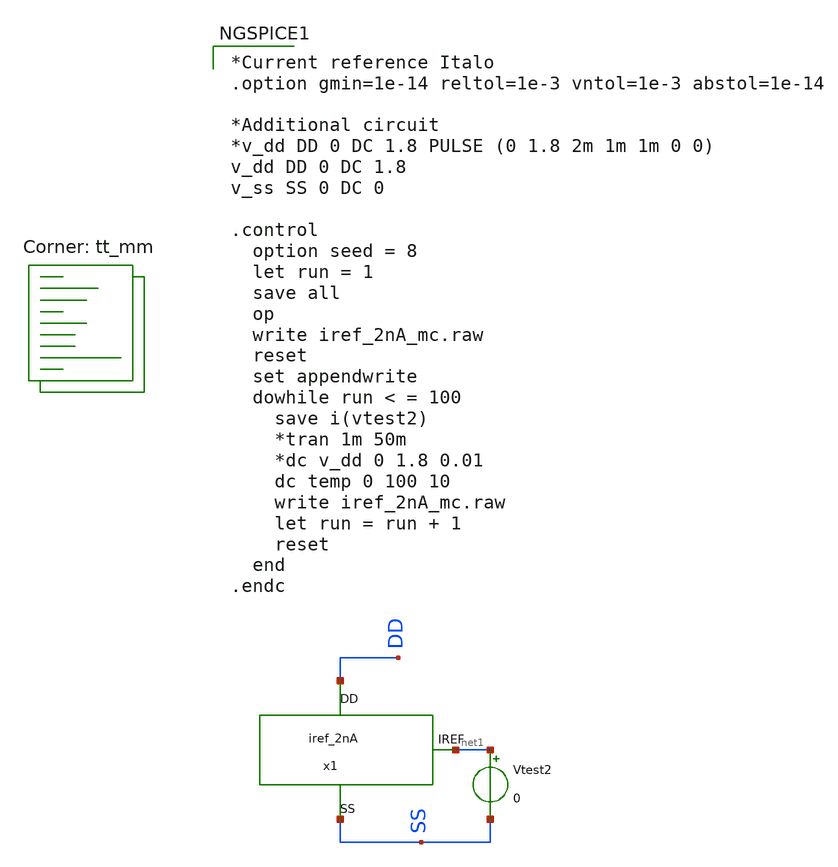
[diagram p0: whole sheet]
** sch_path: xschem/test_iref_2nA_mc.sch
**.subckt test_iref_2nA_mc
x1 net1 DD SS iref_2nA
Vtest2 net1 SS 0
**** begin user architecture code
.lib $::SKYWATER_MODELS/sky130.lib.spice tt_mm

*Current reference Italo
.option gmin=1e-14 reltol=1e-3 vntol=1e-3 abstol=1e-14

*Additional circuit
*v_dd DD 0 DC 1.8 PULSE (0 1.8 2m 1m 1m 0 0)
v_dd DD 0 DC 1.8
v_ss SS 0 DC 0

.control
  option seed = 8
  let run = 1
  save all
  op
  write iref_2nA_mc.raw
  reset
  set appendwrite
  dowhile run < = 100
    save i(vtest2)
    *tran 1m 50m
    *dc v_dd 0 1.8 0.01
    dc temp 0 100 10
    write iref_2nA_mc.raw
    let run = run + 1
    reset
  end
.endc


**** end user architecture code
**.ends

* expanding   symbol:  iref_2nA.sym # of pins=3
** sym_path: xschem/iref_2nA.sym
** sch_path: xschem/iref_2nA.sch
.subckt iref_2nA IREF DD SS
*.iopin DD
*.iopin SS
*.iopin IREF
x1 net3 SS net1 VCTAT net2 iref_2nA_igenerator
x3 DD SS net1 net2 net3 IREF iref_2nA_mirrors
x2 VCTAT DD SS iref_2nA_vref
.ends


* expanding   symbol:  iref_2nA_igenerator.sym # of pins=5
** sym_path: xschem/iref_2nA_igenerator.sym
** sch_path: xschem/iref_2nA_igenerator.sch
.subckt iref_2nA_igenerator Ip2 SS Ip1 VCTAT Vg
*.iopin SS
*.ipin VCTAT
*.iopin Ip1
*.iopin Vg
*.iopin Ip2
XM1 Ip1 Vg VPTAT SS sky130_fd_pr__nfet_01v8_lvt L=1 W=2.5 nf=1 ad='int((nf+1)/2) * W/nf * 0.29' as='int((nf+2)/2) * W/nf * 0.29'
+ pd='2*int((nf+1)/2) * (W/nf + 0.29)' ps='2*int((nf+2)/2) * (W/nf + 0.29)' nrd='0.29 / W' nrs='0.29 / W'
+ sa=0 sb=0 sd=0 mult=2 m=2
XM2 Ip2 Vg SS SS sky130_fd_pr__nfet_01v8_lvt L=1 W=2.5 nf=1 ad='int((nf+1)/2) * W/nf * 0.29' as='int((nf+2)/2) * W/nf * 0.29'
+ pd='2*int((nf+1)/2) * (W/nf + 0.29)' ps='2*int((nf+2)/2) * (W/nf + 0.29)' nrd='0.29 / W' nrs='0.29 / W'
+ sa=0 sb=0 sd=0 mult=2 m=2
XM3 VPTAT VCTAT SS SS sky130_fd_pr__nfet_01v8_lvt L=5 W=1 nf=1 ad='int((nf+1)/2) * W/nf * 0.29' as='int((nf+2)/2) * W/nf * 0.29'
+ pd='2*int((nf+1)/2) * (W/nf + 0.29)' ps='2*int((nf+2)/2) * (W/nf + 0.29)' nrd='0.29 / W' nrs='0.29 / W'
+ sa=0 sb=0 sd=0 mult=1 m=1
XM4 SS SS SS SS sky130_fd_pr__nfet_01v8_lvt L=1 W=2.5 nf=1 ad='int((nf+1)/2) * W/nf * 0.29' as='int((nf+2)/2) * W/nf * 0.29'
+ pd='2*int((nf+1)/2) * (W/nf + 0.29)' ps='2*int((nf+2)/2) * (W/nf + 0.29)' nrd='0.29 / W' nrs='0.29 / W'
+ sa=0 sb=0 sd=0 mult=2 m=2
.ends


* expanding   symbol:  iref_2nA_mirrors.sym # of pins=6
** sym_path: xschem/iref_2nA_mirrors.sym
** sch_path: xschem/iref_2nA_mirrors.sch
.subckt iref_2nA_mirrors DD SS Ip1 Vg Ip2 Iref
*.iopin DD
*.iopin SS
*.iopin Iref
*.iopin Ip2
*.iopin Vg
*.iopin Ip1
XM7 net3 Ip2 DD DD sky130_fd_pr__pfet_01v8_lvt L=2 W=2.5 nf=1 ad='int((nf+1)/2) * W/nf * 0.29' as='int((nf+2)/2) * W/nf * 0.29'
+ pd='2*int((nf+1)/2) * (W/nf + 0.29)' ps='2*int((nf+2)/2) * (W/nf + 0.29)' nrd='0.29 / W' nrs='0.29 / W'
+ sa=0 sb=0 sd=0 mult=10 m=10
XM8 net2 Ip1 DD DD sky130_fd_pr__pfet_01v8_lvt L=2 W=2.5 nf=1 ad='int((nf+1)/2) * W/nf * 0.29' as='int((nf+2)/2) * W/nf * 0.29'
+ pd='2*int((nf+1)/2) * (W/nf + 0.29)' ps='2*int((nf+2)/2) * (W/nf + 0.29)' nrd='0.29 / W' nrs='0.29 / W'
+ sa=0 sb=0 sd=0 mult=2 m=2
XM9 net4 Ip2 DD DD sky130_fd_pr__pfet_01v8_lvt L=2 W=2.5 nf=1 ad='int((nf+1)/2) * W/nf * 0.29' as='int((nf+2)/2) * W/nf * 0.29'
+ pd='2*int((nf+1)/2) * (W/nf + 0.29)' ps='2*int((nf+2)/2) * (W/nf + 0.29)' nrd='0.29 / W' nrs='0.29 / W'
+ sa=0 sb=0 sd=0 mult=2 m=2
XM10 net1 Ip1 DD DD sky130_fd_pr__pfet_01v8_lvt L=2 W=2.5 nf=1 ad='int((nf+1)/2) * W/nf * 0.29' as='int((nf+2)/2) * W/nf * 0.29'
+ pd='2*int((nf+1)/2) * (W/nf + 0.29)' ps='2*int((nf+2)/2) * (W/nf + 0.29)' nrd='0.29 / W' nrs='0.29 / W'
+ sa=0 sb=0 sd=0 mult=2 m=2
XM11 Vn Vn SS SS sky130_fd_pr__nfet_01v8_lvt L=1 W=2.5 nf=1 ad='int((nf+1)/2) * W/nf * 0.29' as='int((nf+2)/2) * W/nf * 0.29'
+ pd='2*int((nf+1)/2) * (W/nf + 0.29)' ps='2*int((nf+2)/2) * (W/nf + 0.29)' nrd='0.29 / W' nrs='0.29 / W'
+ sa=0 sb=0 sd=0 mult=2 m=2
XM12 Vg Vn SS SS sky130_fd_pr__nfet_01v8_lvt L=1 W=2.5 nf=1 ad='int((nf+1)/2) * W/nf * 0.29' as='int((nf+2)/2) * W/nf * 0.29'
+ pd='2*int((nf+1)/2) * (W/nf + 0.29)' ps='2*int((nf+2)/2) * (W/nf + 0.29)' nrd='0.29 / W' nrs='0.29 / W'
+ sa=0 sb=0 sd=0 mult=2 m=2
XM15 net5 Ip2 DD DD sky130_fd_pr__pfet_01v8_lvt L=2 W=2.5 nf=1 ad='int((nf+1)/2) * W/nf * 0.29' as='int((nf+2)/2) * W/nf * 0.29'
+ pd='2*int((nf+1)/2) * (W/nf + 0.29)' ps='2*int((nf+2)/2) * (W/nf + 0.29)' nrd='0.29 / W' nrs='0.29 / W'
+ sa=0 sb=0 sd=0 mult=2 m=2
XM16 Vg Vb net2 DD sky130_fd_pr__pfet_01v8_lvt L=2 W=2.5 nf=1 ad='int((nf+1)/2) * W/nf * 0.29' as='int((nf+2)/2) * W/nf * 0.29'
+ pd='2*int((nf+1)/2) * (W/nf + 0.29)' ps='2*int((nf+2)/2) * (W/nf + 0.29)' nrd='0.29 / W' nrs='0.29 / W'
+ sa=0 sb=0 sd=0 mult=2 m=2
XM17 Ip1 Vb net1 DD sky130_fd_pr__pfet_01v8_lvt L=2 W=2.5 nf=1 ad='int((nf+1)/2) * W/nf * 0.29' as='int((nf+2)/2) * W/nf * 0.29'
+ pd='2*int((nf+1)/2) * (W/nf + 0.29)' ps='2*int((nf+2)/2) * (W/nf + 0.29)' nrd='0.29 / W' nrs='0.29 / W'
+ sa=0 sb=0 sd=0 mult=2 m=2
XM18 Ip2 Vb net3 DD sky130_fd_pr__pfet_01v8_lvt L=2 W=2.5 nf=1 ad='int((nf+1)/2) * W/nf * 0.29' as='int((nf+2)/2) * W/nf * 0.29'
+ pd='2*int((nf+1)/2) * (W/nf + 0.29)' ps='2*int((nf+2)/2) * (W/nf + 0.29)' nrd='0.29 / W' nrs='0.29 / W'
+ sa=0 sb=0 sd=0 mult=10 m=10
XM19 Vn Vb net4 DD sky130_fd_pr__pfet_01v8_lvt L=2 W=2.5 nf=1 ad='int((nf+1)/2) * W/nf * 0.29' as='int((nf+2)/2) * W/nf * 0.29'
+ pd='2*int((nf+1)/2) * (W/nf + 0.29)' ps='2*int((nf+2)/2) * (W/nf + 0.29)' nrd='0.29 / W' nrs='0.29 / W'
+ sa=0 sb=0 sd=0 mult=2 m=2
XM20 Iref Vb net5 DD sky130_fd_pr__pfet_01v8_lvt L=2 W=2.5 nf=1 ad='int((nf+1)/2) * W/nf * 0.29' as='int((nf+2)/2) * W/nf * 0.29'
+ pd='2*int((nf+1)/2) * (W/nf + 0.29)' ps='2*int((nf+2)/2) * (W/nf + 0.29)' nrd='0.29 / W' nrs='0.29 / W'
+ sa=0 sb=0 sd=0 mult=2 m=2
XM22 net6 net6 DD DD sky130_fd_pr__pfet_01v8_lvt L=2 W=2.5 nf=1 ad='int((nf+1)/2) * W/nf * 0.29' as='int((nf+2)/2) * W/nf * 0.29'
+ pd='2*int((nf+1)/2) * (W/nf + 0.29)' ps='2*int((nf+2)/2) * (W/nf + 0.29)' nrd='0.29 / W' nrs='0.29 / W'
+ sa=0 sb=0 sd=0 mult=2 m=2
XM21 Vb Vn SS SS sky130_fd_pr__nfet_01v8_lvt L=1 W=2.5 nf=1 ad='int((nf+1)/2) * W/nf * 0.29' as='int((nf+2)/2) * W/nf * 0.29'
+ pd='2*int((nf+1)/2) * (W/nf + 0.29)' ps='2*int((nf+2)/2) * (W/nf + 0.29)' nrd='0.29 / W' nrs='0.29 / W'
+ sa=0 sb=0 sd=0 mult=2 m=2
XM23 Vb Vb net6 DD sky130_fd_pr__pfet_01v8_lvt L=2 W=2.5 nf=1 ad='int((nf+1)/2) * W/nf * 0.29' as='int((nf+2)/2) * W/nf * 0.29'
+ pd='2*int((nf+1)/2) * (W/nf + 0.29)' ps='2*int((nf+2)/2) * (W/nf + 0.29)' nrd='0.29 / W' nrs='0.29 / W'
+ sa=0 sb=0 sd=0 mult=2 m=2
XM1 DD DD DD DD sky130_fd_pr__pfet_01v8_lvt L=2 W=0.5 nf=1 ad='int((nf+1)/2) * W/nf * 0.29' as='int((nf+2)/2) * W/nf * 0.29'
+ pd='2*int((nf+1)/2) * (W/nf + 0.29)' ps='2*int((nf+2)/2) * (W/nf + 0.29)' nrd='0.29 / W' nrs='0.29 / W'
+ sa=0 sb=0 sd=0 mult=8 m=8
XM2 SS SS SS SS sky130_fd_pr__nfet_01v8_lvt L=1 W=2.5 nf=1 ad='int((nf+1)/2) * W/nf * 0.29' as='int((nf+2)/2) * W/nf * 0.29'
+ pd='2*int((nf+1)/2) * (W/nf + 0.29)' ps='2*int((nf+2)/2) * (W/nf + 0.29)' nrd='0.29 / W' nrs='0.29 / W'
+ sa=0 sb=0 sd=0 mult=2 m=2
.ends


* expanding   symbol:  iref_2nA_vref.sym # of pins=3
** sym_path: xschem/iref_2nA_vref.sym
** sch_path: xschem/iref_2nA_vref.sch
.subckt iref_2nA_vref VREF DD SS
*.iopin DD
*.iopin SS
*.iopin VREF
XM1 N2 N1 DD DD sky130_fd_pr__pfet_01v8 L=4.38 W=2.37 nf=1 ad='int((nf+1)/2) * W/nf * 0.29' as='int((nf+2)/2) * W/nf * 0.29'
+ pd='2*int((nf+1)/2) * (W/nf + 0.29)' ps='2*int((nf+2)/2) * (W/nf + 0.29)' nrd='0.29 / W' nrs='0.29 / W'
+ sa=0 sb=0 sd=0 mult=1 m=1
XM2 SS N2 N2 N2 sky130_fd_pr__pfet_01v8_lvt L=6.97 W=0.88 nf=1 ad='int((nf+1)/2) * W/nf * 0.29' as='int((nf+2)/2) * W/nf * 0.29'
+ pd='2*int((nf+1)/2) * (W/nf + 0.29)' ps='2*int((nf+2)/2) * (W/nf + 0.29)' nrd='0.29 / W' nrs='0.29 / W'
+ sa=0 sb=0 sd=0 mult=1 m=1
XM3 N1 DD DD DD sky130_fd_pr__pfet_01v8_lvt L=4 W=0.5 nf=1 ad='int((nf+1)/2) * W/nf * 0.29' as='int((nf+2)/2) * W/nf * 0.29'
+ pd='2*int((nf+1)/2) * (W/nf + 0.29)' ps='2*int((nf+2)/2) * (W/nf + 0.29)' nrd='0.29 / W' nrs='0.29 / W'
+ sa=0 sb=0 sd=0 mult=1 m=1
XM4 VREF N2 N1 DD sky130_fd_pr__pfet_01v8_lvt L=2.77 W=3.43 nf=1 ad='int((nf+1)/2) * W/nf * 0.29' as='int((nf+2)/2) * W/nf * 0.29'
+ pd='2*int((nf+1)/2) * (W/nf + 0.29)' ps='2*int((nf+2)/2) * (W/nf + 0.29)' nrd='0.29 / W' nrs='0.29 / W'
+ sa=0 sb=0 sd=0 mult=1 m=1
XM5 SS SS VREF VREF sky130_fd_pr__pfet_01v8 L=0.5 W=2 nf=1 ad='int((nf+1)/2) * W/nf * 0.29' as='int((nf+2)/2) * W/nf * 0.29'
+ pd='2*int((nf+1)/2) * (W/nf + 0.29)' ps='2*int((nf+2)/2) * (W/nf + 0.29)' nrd='0.29 / W' nrs='0.29 / W'
+ sa=0 sb=0 sd=0 mult=4 m=4
.ends

.end
